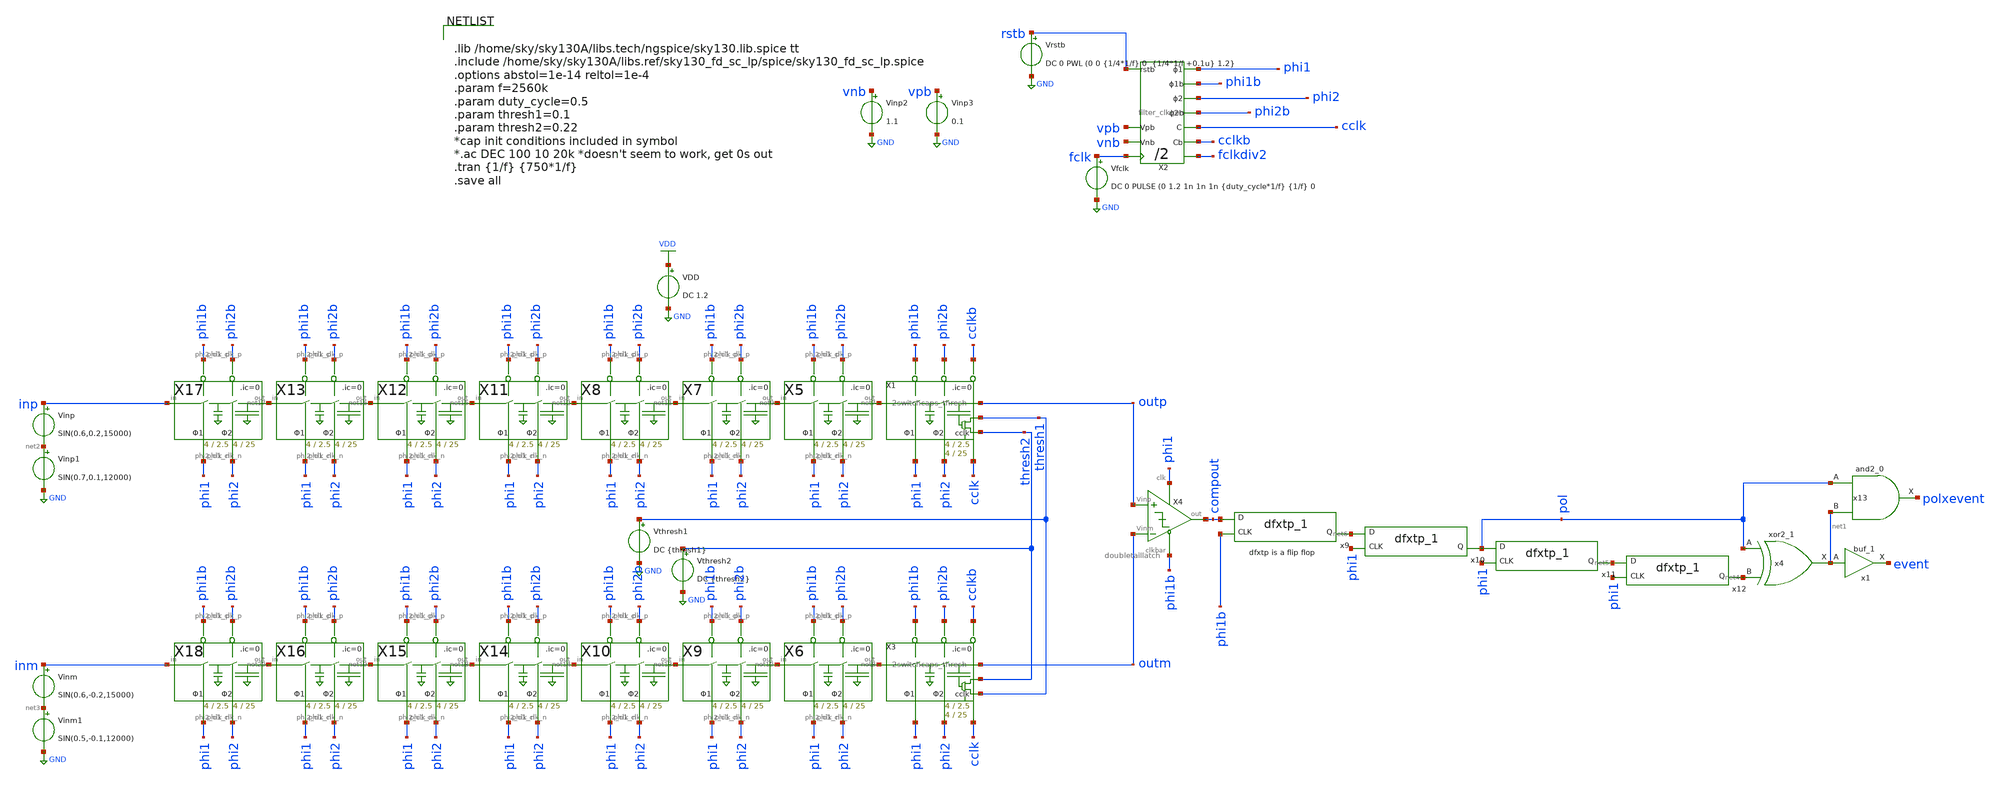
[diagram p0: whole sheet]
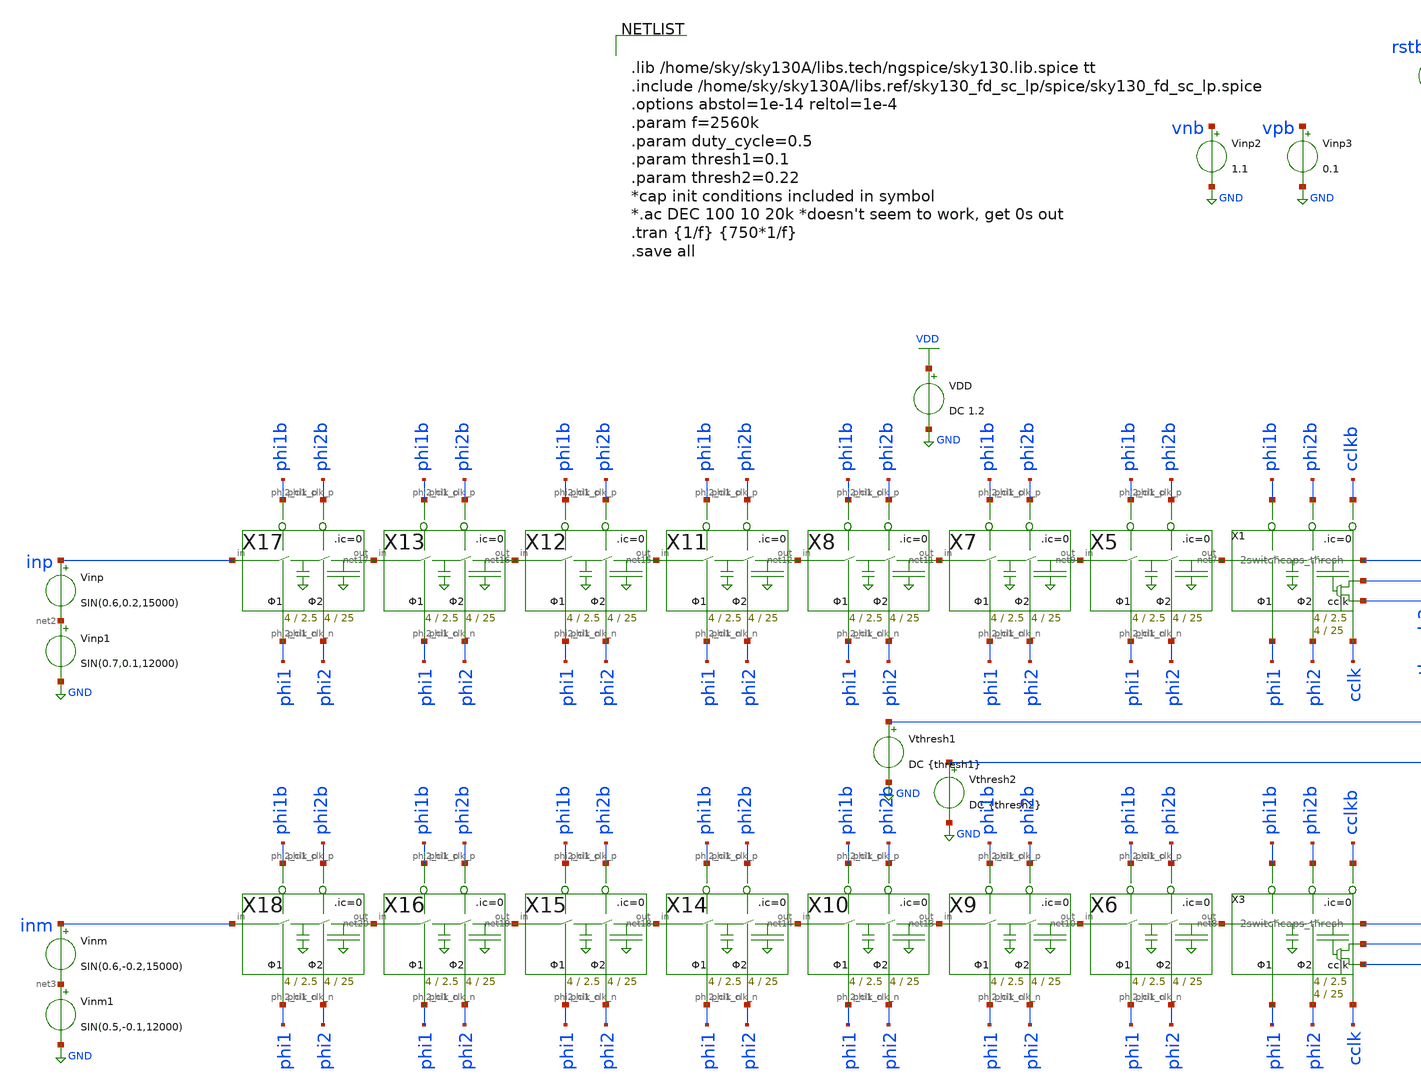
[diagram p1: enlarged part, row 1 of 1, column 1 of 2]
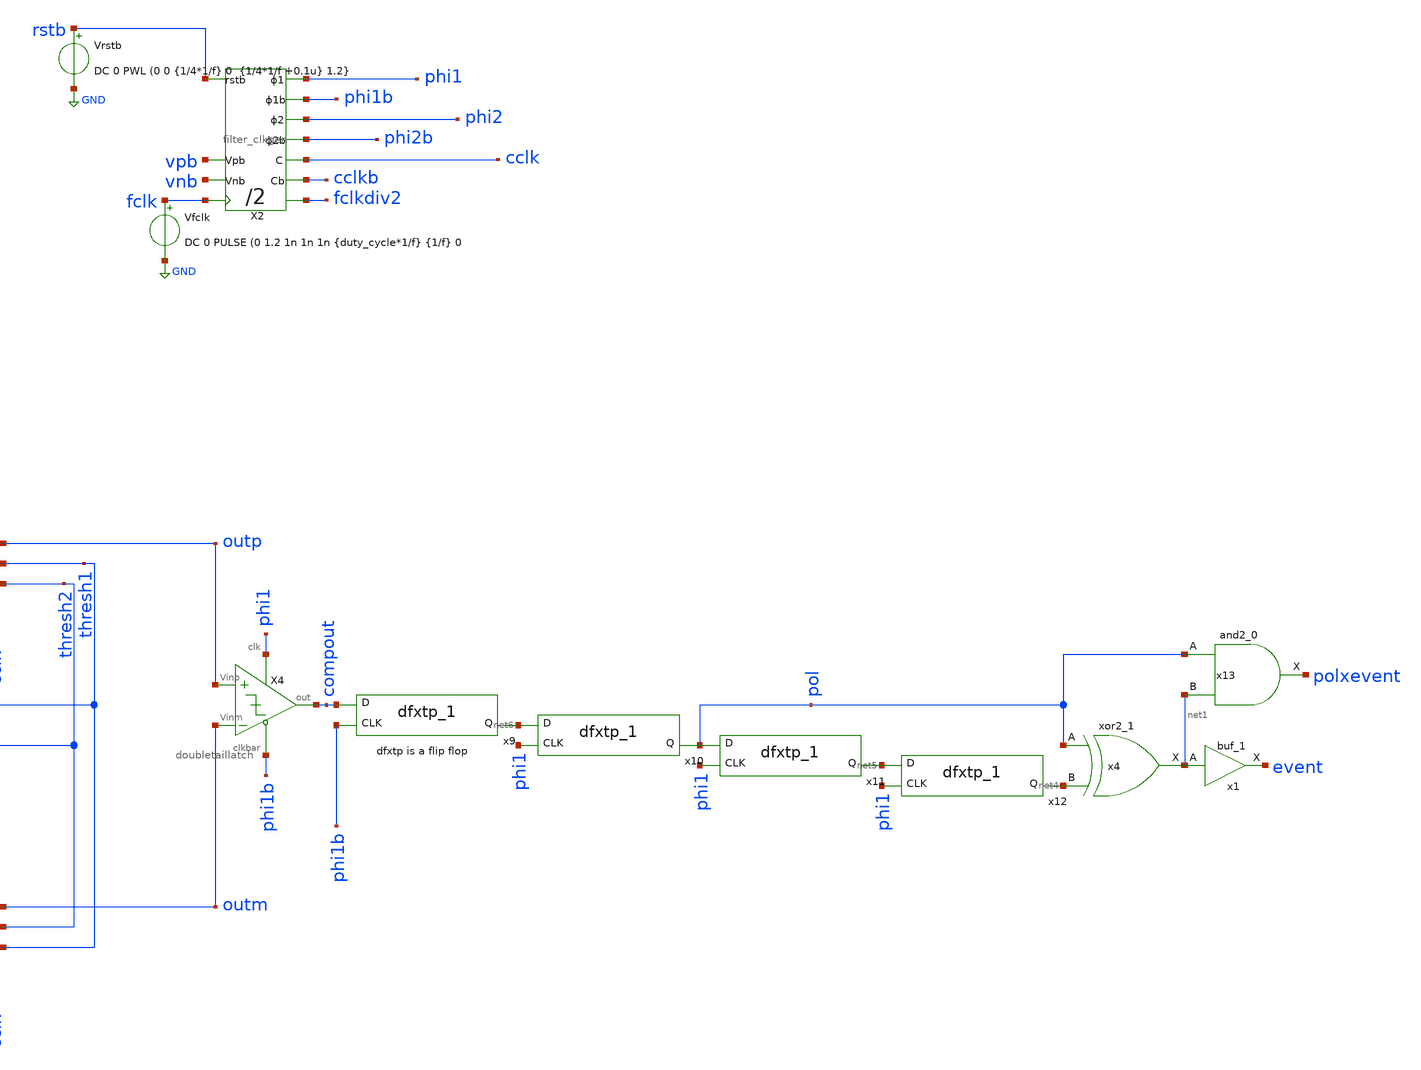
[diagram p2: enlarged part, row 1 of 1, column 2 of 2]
** sch_path: xschem/comparator/2switchcaps_thresh_tb.sch
**.subckt 2switchcaps_thresh_tb
Vinp inp net2 SIN(0.6,0.2,15000)
VDD VDD GND DC 1.2
Vfclk fclk GND DC 0 PULSE (0 1.2 1n 1n 1n {duty_cycle*1/f} {1/f} 0
X2 rstb fclk phi2b phi2 phi1b phi1 cclkb cclk fclkdiv2 vpb vnb filter_clkgen
Vthresh1 thresh1 GND DC {thresh1}
Vthresh2 thresh2 GND DC {thresh2}
Vrstb rstb GND DC 0 PWL (0 0 {1/4*1/f} 0 {1/4*1/f +0.1u} 1.2}
Vinm inm net3 SIN(0.6,-0.2,15000)
X4 outp outm compout phi1 phi1b doubletaillatch
Vinp1 net2 GND SIN(0.7,0.1,12000)
Vinm1 net3 GND SIN(0.5,-0.1,12000)
x4 pol net4 GND GND VDD VDD net1 sky130_fd_sc_lp__xor2_1
x11 phi1 pol gnd gnd vdd vdd net5 sky130_fd_sc_lp__dfxtp_1
x12 phi1 net5 gnd gnd vdd vdd net4 sky130_fd_sc_lp__dfxtp_1
x9 phi1b compout gnd gnd vdd vdd net6 sky130_fd_sc_lp__dfxtp_1
x10 phi1 net6 gnd gnd vdd vdd pol sky130_fd_sc_lp__dfxtp_1
x13 pol net1 GND GND VDD VDD polxevent sky130_fd_sc_lp__and2_0
X1 net7 outp phi2 phi1 phi1b phi2b thresh2 cclk thresh1 cclkb 2switchcaps_thresh Wcap1=4 Lcap1=2.5 Wcap2=4 Lcap2=25
X3 net8 outm phi2 phi1 phi1b phi2b thresh1 cclk thresh2 cclkb 2switchcaps_thresh Wcap1=4 Lcap1=2.5 Wcap2=4 Lcap2=25
X5 net9 net7 phi2 phi1 phi1b phi2b 2switchcaps Wcap1=4 Lcap1=2.5 Wcap2=4 Lcap2=25
X6 net10 net8 phi2 phi1 phi1b phi2b 2switchcaps Wcap1=4 Lcap1=2.5 Wcap2=4 Lcap2=25
X7 net11 net9 phi2 phi1 phi1b phi2b 2switchcaps Wcap1=4 Lcap1=2.5 Wcap2=4 Lcap2=25
X8 net12 net11 phi2 phi1 phi1b phi2b 2switchcaps Wcap1=4 Lcap1=2.5 Wcap2=4 Lcap2=25
X9 net13 net10 phi2 phi1 phi1b phi2b 2switchcaps Wcap1=4 Lcap1=2.5 Wcap2=4 Lcap2=25
X10 net14 net13 phi2 phi1 phi1b phi2b 2switchcaps Wcap1=4 Lcap1=2.5 Wcap2=4 Lcap2=25
x1 net1 GND GND VDD VDD event sky130_fd_sc_lp__buf_1
X11 net15 net12 phi2 phi1 phi1b phi2b 2switchcaps Wcap1=4 Lcap1=2.5 Wcap2=4 Lcap2=25
X12 net16 net15 phi2 phi1 phi1b phi2b 2switchcaps Wcap1=4 Lcap1=2.5 Wcap2=4 Lcap2=25
X13 net17 net16 phi2 phi1 phi1b phi2b 2switchcaps Wcap1=4 Lcap1=2.5 Wcap2=4 Lcap2=25
X14 net18 net14 phi2 phi1 phi1b phi2b 2switchcaps Wcap1=4 Lcap1=2.5 Wcap2=4 Lcap2=25
X15 net19 net18 phi2 phi1 phi1b phi2b 2switchcaps Wcap1=4 Lcap1=2.5 Wcap2=4 Lcap2=25
X16 net20 net19 phi2 phi1 phi1b phi2b 2switchcaps Wcap1=4 Lcap1=2.5 Wcap2=4 Lcap2=25
X17 inp net17 phi2 phi1 phi1b phi2b 2switchcaps Wcap1=4 Lcap1=2.5 Wcap2=4 Lcap2=25
X18 inm net20 phi2 phi1 phi1b phi2b 2switchcaps Wcap1=4 Lcap1=2.5 Wcap2=4 Lcap2=25
Vinp2 vnb GND 1.1
Vinp3 vpb GND 0.1
**** begin user architecture code


.lib /home/sky/sky130A/libs.tech/ngspice/sky130.lib.spice tt
.include /home/sky/sky130A/libs.ref/sky130_fd_sc_lp/spice/sky130_fd_sc_lp.spice
.options abstol=1e-14 reltol=1e-4
.param f=2560k
.param duty_cycle=0.5
.param thresh1=0.1
.param thresh2=0.22
*cap init conditions included in symbol
*.ac DEC 100 10 20k *doesn't seem to work, get 0s out
.tran {1/f} {750*1/f}
.save all


**** end user architecture code
**.ends
.GLOBAL GND
.GLOBAL VDD
.end
